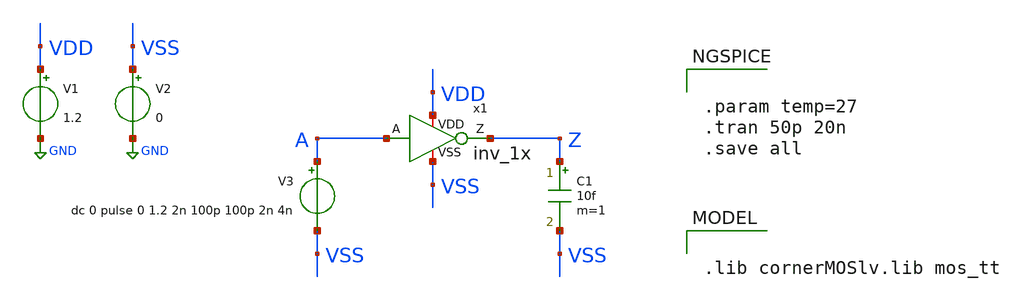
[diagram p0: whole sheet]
** sch_path: analog/tb/tb_inv_1x.sch
**.subckt tb_inv_1x
V1 VDD GND 1.2
C1 Z VSS 10f m=1
V2 VSS GND 0
x1 VDD A Z VSS inv_1x
V3 A VSS dc 0 pulse 0 1.2 2n 100p 100p 2n 4n
**** begin user architecture code


.param temp=27
.tran 50p 20n
.save all




.lib cornerMOSlv.lib mos_tt


**** end user architecture code
**.ends
.GLOBAL GND
.end
